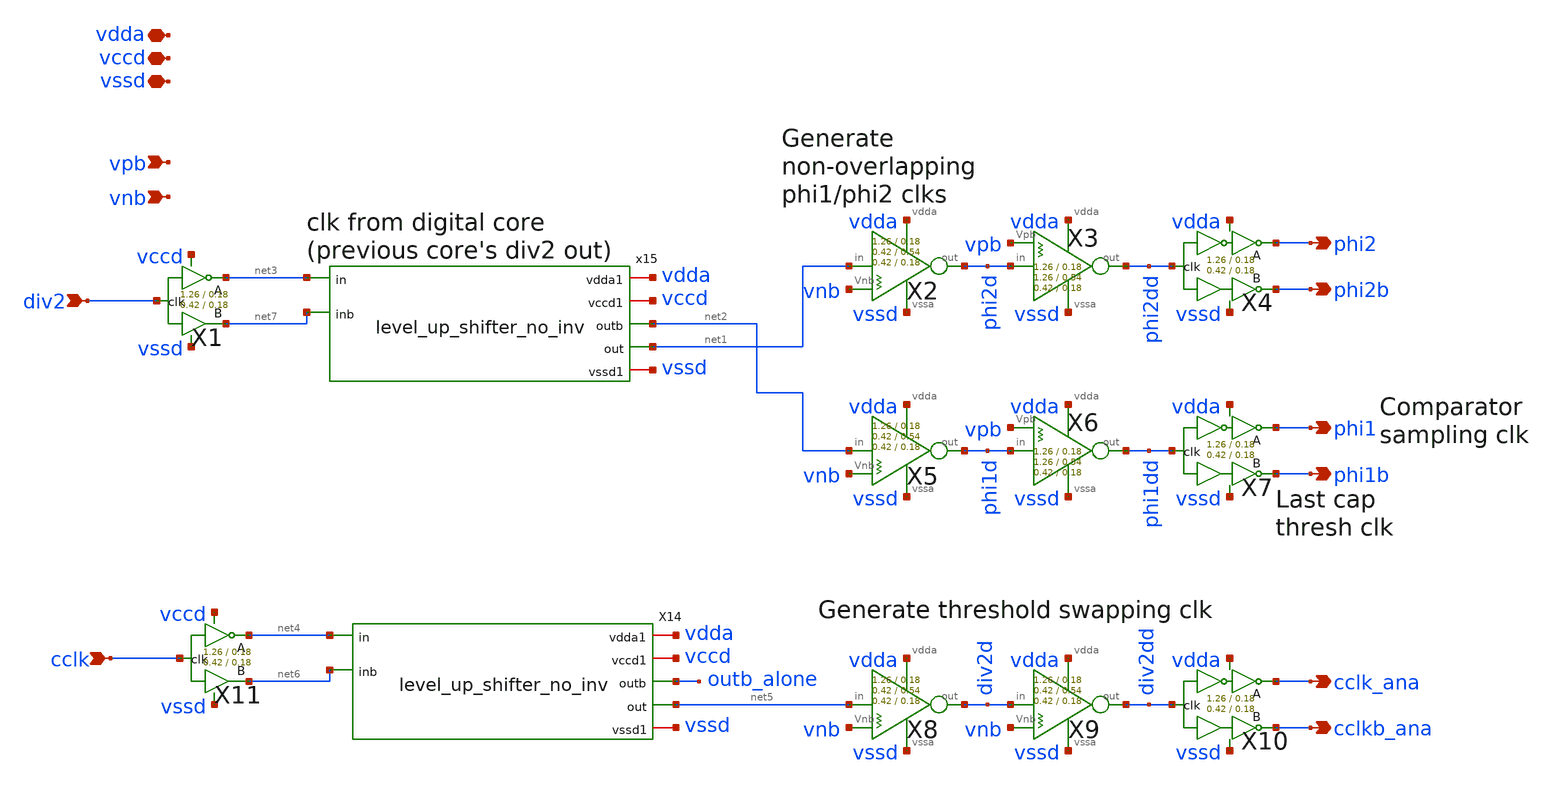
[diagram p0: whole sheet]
** sch_path: xschem/clkgen/filter_clkgen_balanced_clks.sch
**.subckt filter_clkgen_balanced_clks div2 phi2 phi2b phi1 phi1b cclk_ana cclkb_ana vpb vnb cclk
*+ vdda vccd vssd
*.ipin div2
*.opin phi2
*.opin phi2b
*.opin phi1
*.opin phi1b
*.opin cclk_ana
*.opin cclkb_ana
*.ipin vpb
*.ipin vnb
*.ipin cclk
*.iopin vdda
*.iopin vccd
*.iopin vssd
X4 phi2dd phi2 phi2b vdda vssd comp_clks Wpmos=1.26 Lpmos=0.18 Wnmos=0.42 Lnmos=0.18
X7 phi1dd phi1 phi1b vdda vssd comp_clks Wpmos=1.26 Lpmos=0.18 Wnmos=0.42 Lnmos=0.18
X10 div2dd cclk_ana cclkb_ana vdda vssd comp_clks Wpmos=1.26 Lpmos=0.18 Wnmos=0.42 Lnmos=0.18
X1 div2 net3 net7 vccd vssd comp_clks_1stage Wpmos=1.26 Lpmos=0.18 Wnmos=0.42 Lnmos=0.18
X2 net1 phi2d vnb vdda vssd inv_weak_pulldown Wpmos=1.26 Lpmos= Wnmos= Lnmos=0.54
X5 net2 phi1d vnb vdda vssd inv_weak_pulldown Wpmos=1.26 Lpmos= Wnmos= Lnmos=0.54
X8 net5 div2d vnb vdda vssd inv_weak_pulldown Wpmos=1.26 Lpmos= Wnmos= Lnmos=0.54
X9 div2d div2dd vnb vdda vssd inv_weak_pulldown Wpmos=1.26 Lpmos= Wnmos= Lnmos=0.54
X3 phi2d phi2dd vpb vdda vssd inv_weak_pullup Wpmos=1.26 Lpmos=0.54 Wnmos= Lnmos=
X6 phi1d phi1dd vpb vdda vssd inv_weak_pullup Wpmos=1.26 Lpmos=0.54 Wnmos= Lnmos=
X11 cclk net4 net6 vccd vssd comp_clks_1stage Wpmos=1.26 Lpmos=0.18 Wnmos=0.42 Lnmos=0.18
x15 vdda vccd net3 net2 net1 vssd net7 level_up_shifter_no_inv
X14 vdda vccd net4 outb_alone net5 vssd net6 level_up_shifter_no_inv
**.ends

* expanding   symbol:  clkgen/comp_clks.sym # of pins=5
** sym_path: xschem/clkgen/comp_clks.sym
** sch_path: xschem/clkgen/comp_clks.sch
.subckt comp_clks clk clka clkb vdd vss  Wpmos=Wpmos Lpmos=Lpmos Wnmos=Wnmos Lnmos=Lnmos
*.ipin clk
*.opin clka
*.opin clkb
*.iopin vdd
*.iopin vss
X1 clk clki vdd vss inv Wpmos=Wpmos Lpmos=Lpmos Wnmos=Wnmos Lnmos=Lnmos
X2 clki clka vdd vss inv Wpmos=Wpmos Lpmos=Lpmos Wnmos=Wnmos Lnmos=Lnmos
X4 clkt clkb vdd vss inv Wpmos=Wpmos Lpmos=Lpmos Wnmos=Wnmos Lnmos=Lnmos
x3 clk clkt vss vdd vdd vss tg Wpmos=Wpmos Lpmos=Lpmos Wnmos=Wnmos Lnmos=Lnmos
.ends


* expanding   symbol:  clkgen/comp_clks_1stage.sym # of pins=5
** sym_path: xschem/clkgen/comp_clks_1stage.sym
** sch_path: xschem/clkgen/comp_clks_1stage.sch
.subckt comp_clks_1stage clk clka clkb vdd vss  Wpmos=1.26 Lpmos=0.18 Wnmos=0.42 Lnmos=0.18
*.ipin clk
*.opin clka
*.opin clkb
*.iopin vdd
*.iopin vss
X1 clk clka vdd vss inv Wpmos=Wpmos Lpmos=Lpmos Wnmos=Wnmos Lnmos=Lnmos
x2 clk clkb vss vdd vdd vss tg Wpmos=0.63 Lpmos=0.18 Wnmos=0.42 Lnmos=0.18
.ends


* expanding   symbol:  inv/inv_weak_pulldown.sym # of pins=5
** sym_path: xschem/inv/inv_weak_pulldown.sym
** sch_path: xschem/inv/inv_weak_pulldown.sch
.subckt inv_weak_pulldown in out Vnb vdda vssa  Wpmos=1.26 Lmin=0.18 Wmin=0.42 Lnmos=0.54
*.ipin in
*.iopin out
*.ipin Vnb
*.ipin vdda
*.ipin vssa
XM1 net1 in vssa vssa sky130_fd_pr__nfet_01v8 L=Lmin W=Wmin nf=1 ad='int((nf+1)/2) * W/nf * 0.29' as='int((nf+2)/2) * W/nf * 0.29'
+ pd='2*int((nf+1)/2) * (W/nf + 0.29)' ps='2*int((nf+2)/2) * (W/nf + 0.29)' nrd='0.29 / W' nrs='0.29 / W'
+ sa=0 sb=0 sd=0 mult=1 m=1
XM3 out Vnb net1 vssa sky130_fd_pr__nfet_01v8 L=Lnmos W=Wmin nf=1 ad='int((nf+1)/2) * W/nf * 0.29' as='int((nf+2)/2) * W/nf * 0.29'
+ pd='2*int((nf+1)/2) * (W/nf + 0.29)' ps='2*int((nf+2)/2) * (W/nf + 0.29)' nrd='0.29 / W' nrs='0.29 / W'
+ sa=0 sb=0 sd=0 mult=1 m=1
XM4 out in vdda vdda sky130_fd_pr__pfet_01v8 L=Lmin W=Wpmos nf=1 ad='int((nf+1)/2) * W/nf * 0.29' as='int((nf+2)/2) * W/nf * 0.29'
+ pd='2*int((nf+1)/2) * (W/nf + 0.29)' ps='2*int((nf+2)/2) * (W/nf + 0.29)' nrd='0.29 / W' nrs='0.29 / W'
+ sa=0 sb=0 sd=0 mult=1 m=1
.ends


* expanding   symbol:  inv/inv_weak_pullup.sym # of pins=5
** sym_path: xschem/inv/inv_weak_pullup.sym
** sch_path: xschem/inv/inv_weak_pullup.sch
.subckt inv_weak_pullup in out Vpb vdda vssa  Wpmos=1.26 Lpmos=0.54 Wmin=0.42 Lmin=0.18
*.ipin in
*.iopin out
*.ipin Vpb
*.ipin vdda
*.ipin vssa
XM1 out in vssa vssa sky130_fd_pr__nfet_01v8 L=Lmin W=Wmin nf=1 ad='int((nf+1)/2) * W/nf * 0.29' as='int((nf+2)/2) * W/nf * 0.29'
+ pd='2*int((nf+1)/2) * (W/nf + 0.29)' ps='2*int((nf+2)/2) * (W/nf + 0.29)' nrd='0.29 / W' nrs='0.29 / W'
+ sa=0 sb=0 sd=0 mult=1 m=1
XM3 out Vpb net1 vdda sky130_fd_pr__pfet_01v8 L=Lmin W=Wpmos nf=1 ad='int((nf+1)/2) * W/nf * 0.29' as='int((nf+2)/2) * W/nf * 0.29'
+ pd='2*int((nf+1)/2) * (W/nf + 0.29)' ps='2*int((nf+2)/2) * (W/nf + 0.29)' nrd='0.29 / W' nrs='0.29 / W'
+ sa=0 sb=0 sd=0 mult=1 m=1
XM5 net1 in vdda vdda sky130_fd_pr__pfet_01v8 L=Lmin W=Wpmos nf=1 ad='int((nf+1)/2) * W/nf * 0.29' as='int((nf+2)/2) * W/nf * 0.29'
+ pd='2*int((nf+1)/2) * (W/nf + 0.29)' ps='2*int((nf+2)/2) * (W/nf + 0.29)' nrd='0.29 / W' nrs='0.29 / W'
+ sa=0 sb=0 sd=0 mult=1 m=1
.ends


* expanding   symbol:  level_shifter/level_up_shifter_no_inv.sym # of pins=7
** sym_path: xschem/level_shifter/level_up_shifter_no_inv.sym
** sch_path: xschem/level_shifter/level_up_shifter_no_inv.sch
.subckt level_up_shifter_no_inv vdda1 vccd1 in outb out vssd1 inb
*.ipin in
*.iopin vdda1
*.opin out
*.opin outb
*.ipin inb
*.iopin vssd1
*.iopin vccd1
XM7 outb out vdda1 vdda1 sky130_fd_pr__pfet_01v8 L=0.15 W=0.42 nf=1 ad='int((nf+1)/2) * W/nf * 0.29'
+ as='int((nf+2)/2) * W/nf * 0.29' pd='2*int((nf+1)/2) * (W/nf + 0.29)' ps='2*int((nf+2)/2) * (W/nf + 0.29)'
+ nrd='0.29 / W' nrs='0.29 / W' sa=0 sb=0 sd=0 mult=1 m=1
XM8 out outb vdda1 vdda1 sky130_fd_pr__pfet_01v8 L=0.15 W=0.42 nf=1 ad='int((nf+1)/2) * W/nf * 0.29'
+ as='int((nf+2)/2) * W/nf * 0.29' pd='2*int((nf+1)/2) * (W/nf + 0.29)' ps='2*int((nf+2)/2) * (W/nf + 0.29)'
+ nrd='0.29 / W' nrs='0.29 / W' sa=0 sb=0 sd=0 mult=1 m=1
XM2 outb inb vdda1 vssd1 sky130_fd_pr__nfet_01v8 L=0.15 W=0.6 nf=1 ad='int((nf+1)/2) * W/nf * 0.29' as='int((nf+2)/2) * W/nf * 0.29'
+ pd='2*int((nf+1)/2) * (W/nf + 0.29)' ps='2*int((nf+2)/2) * (W/nf + 0.29)' nrd='0.29 / W' nrs='0.29 / W'
+ sa=0 sb=0 sd=0 mult=4 m=4
XM3 outb in vssd1 vssd1 sky130_fd_pr__nfet_01v8 L=0.15 W=0.6 nf=1 ad='int((nf+1)/2) * W/nf * 0.29' as='int((nf+2)/2) * W/nf * 0.29'
+ pd='2*int((nf+1)/2) * (W/nf + 0.29)' ps='2*int((nf+2)/2) * (W/nf + 0.29)' nrd='0.29 / W' nrs='0.29 / W'
+ sa=0 sb=0 sd=0 mult=4 m=4
XM4 vssd1 in outb vssd1 sky130_fd_pr__nfet_01v8 L=0.15 W=0.6 nf=1 ad='int((nf+1)/2) * W/nf * 0.29' as='int((nf+2)/2) * W/nf * 0.29'
+ pd='2*int((nf+1)/2) * (W/nf + 0.29)' ps='2*int((nf+2)/2) * (W/nf + 0.29)' nrd='0.29 / W' nrs='0.29 / W'
+ sa=0 sb=0 sd=0 mult=4 m=4
XM5 out inb vssd1 vssd1 sky130_fd_pr__nfet_01v8 L=0.15 W=0.6 nf=1 ad='int((nf+1)/2) * W/nf * 0.29' as='int((nf+2)/2) * W/nf * 0.29'
+ pd='2*int((nf+1)/2) * (W/nf + 0.29)' ps='2*int((nf+2)/2) * (W/nf + 0.29)' nrd='0.29 / W' nrs='0.29 / W'
+ sa=0 sb=0 sd=0 mult=4 m=4
XM6 vssd1 inb out vssd1 sky130_fd_pr__nfet_01v8 L=0.15 W=0.6 nf=1 ad='int((nf+1)/2) * W/nf * 0.29' as='int((nf+2)/2) * W/nf * 0.29'
+ pd='2*int((nf+1)/2) * (W/nf + 0.29)' ps='2*int((nf+2)/2) * (W/nf + 0.29)' nrd='0.29 / W' nrs='0.29 / W'
+ sa=0 sb=0 sd=0 mult=4 m=4
XM9 vdda1 in out vssd1 sky130_fd_pr__nfet_01v8 L=0.15 W=0.6 nf=1 ad='int((nf+1)/2) * W/nf * 0.29' as='int((nf+2)/2) * W/nf * 0.29'
+ pd='2*int((nf+1)/2) * (W/nf + 0.29)' ps='2*int((nf+2)/2) * (W/nf + 0.29)' nrd='0.29 / W' nrs='0.29 / W'
+ sa=0 sb=0 sd=0 mult=4 m=4
XM10 out in vdda1 vssd1 sky130_fd_pr__nfet_01v8 L=0.15 W=0.6 nf=1 ad='int((nf+1)/2) * W/nf * 0.29' as='int((nf+2)/2) * W/nf * 0.29'
+ pd='2*int((nf+1)/2) * (W/nf + 0.29)' ps='2*int((nf+2)/2) * (W/nf + 0.29)' nrd='0.29 / W' nrs='0.29 / W'
+ sa=0 sb=0 sd=0 mult=4 m=4
XM11 vdda1 inb outb vssd1 sky130_fd_pr__nfet_01v8 L=0.15 W=0.6 nf=1 ad='int((nf+1)/2) * W/nf * 0.29'
+ as='int((nf+2)/2) * W/nf * 0.29' pd='2*int((nf+1)/2) * (W/nf + 0.29)' ps='2*int((nf+2)/2) * (W/nf + 0.29)'
+ nrd='0.29 / W' nrs='0.29 / W' sa=0 sb=0 sd=0 mult=4 m=4
.ends


* expanding   symbol:  xschem/inv/inv.sym # of pins=4
** sym_path: xschem/inv/inv.sym
** sch_path: xschem/inv/inv.sch
.subckt inv in out vdd vss  Wpmos=Wpmos Lpmos=Lpmos Wnmos=Wnmos Lnmos=Lnmos
*.ipin in
*.iopin out
*.iopin vdd
*.iopin vss
XM1 vss in out vss sky130_fd_pr__nfet_01v8 L=Lnmos W=Wnmos nf=1 ad='int((nf+1)/2) * W/nf * 0.29' as='int((nf+2)/2) * W/nf * 0.29'
+ pd='2*int((nf+1)/2) * (W/nf + 0.29)' ps='2*int((nf+2)/2) * (W/nf + 0.29)' nrd='0.29 / W' nrs='0.29 / W'
+ sa=0 sb=0 sd=0 mult=1 m=1
XM2 vdd in out vdd sky130_fd_pr__pfet_01v8 L=Lpmos W=Wpmos nf=1 ad='int((nf+1)/2) * W/nf * 0.29' as='int((nf+2)/2) * W/nf * 0.29'
+ pd='2*int((nf+1)/2) * (W/nf + 0.29)' ps='2*int((nf+2)/2) * (W/nf + 0.29)' nrd='0.29 / W' nrs='0.29 / W'
+ sa=0 sb=0 sd=0 mult=1 m=1
.ends


* expanding   symbol:  xschem/transmission_gate/tg.sym # of pins=6
** sym_path: xschem/transmission_gate/tg.sym
** sch_path: xschem/transmission_gate/tg.sch
.subckt tg in out ctrl_ ctrl vdda vssa  Wpmos=0.42 Lpmos=0.18 Wnmos=0.42 Lnmos=0.18
*.iopin in
*.iopin out
*.ipin ctrl_
*.ipin ctrl
*.ipin vdda
*.ipin vssa
XM1 out ctrl in vssa sky130_fd_pr__nfet_01v8 L=Lnmos W=Wnmos nf=1 ad='int((nf+1)/2) * W/nf * 0.29' as='int((nf+2)/2) * W/nf * 0.29'
+ pd='2*int((nf+1)/2) * (W/nf + 0.29)' ps='2*int((nf+2)/2) * (W/nf + 0.29)' nrd='0.29 / W' nrs='0.29 / W'
+ sa=0 sb=0 sd=0 mult=1 m=1
XM2 out ctrl_ in vdda sky130_fd_pr__pfet_01v8 L=Lpmos W=Wpmos nf=1 ad='int((nf+1)/2) * W/nf * 0.29' as='int((nf+2)/2) * W/nf * 0.29'
+ pd='2*int((nf+1)/2) * (W/nf + 0.29)' ps='2*int((nf+2)/2) * (W/nf + 0.29)' nrd='0.29 / W' nrs='0.29 / W'
+ sa=0 sb=0 sd=0 mult=2 m=2
.ends

.end
